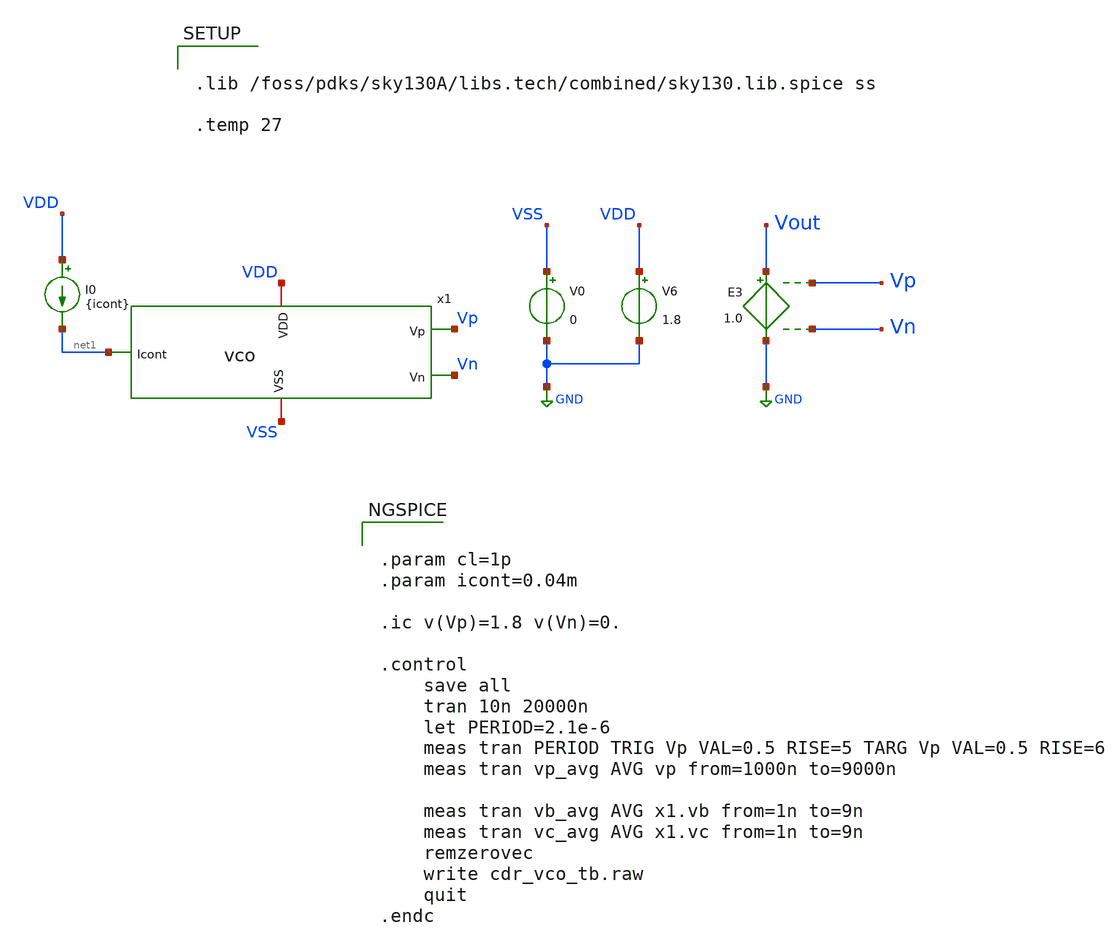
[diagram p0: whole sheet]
** sch_path: xschem/vco_tb.sch
**.subckt vco_tb
V0 VSS GND 0
V6 VDD GND 1.8
I0 VDD net1 {icont}
E3 Vout GND Vp Vn 1.0
x1 VDD VSS net1 Vp Vn vco
**** begin user architecture code


.param cl=1p
.param icont=0.04m

.ic v(Vp)=1.8 v(Vn)=0.

.control
	save all
	tran 10n 20000n
	let PERIOD=2.1e-6
	meas tran PERIOD TRIG Vp VAL=0.5 RISE=5 TARG Vp VAL=0.5 RISE=6
	meas tran vp_avg AVG vp from=1000n to=9000n

	meas tran vb_avg AVG x1.vb from=1n to=9n
	meas tran vc_avg AVG x1.vc from=1n to=9n
	remzerovec
	write cdr_vco_tb.raw
	quit
.endc




.lib /foss/pdks/sky130A/libs.tech/combined/sky130.lib.spice ss

.temp 27


**** end user architecture code
**.ends

* expanding   symbol:  vco.sym # of pins=5
** sym_path: xschem/vco.sym
** sch_path: xschem/vco.sch
.subckt vco VDD VSS Icont Vp Vn
*.iopin VDD
*.iopin VSS
*.ipin Icont
*.opin Vp
*.opin Vn
x1 VDD VSS Vp Vn Vb Vc net1 net2 vco_stage
x2 VDD VSS net1 net2 Vb Vc net3 net4 vco_stage
x3 VDD VSS net3 net4 Vb Vc Vpin1 Vnin1 vco_stage
x4 VDD VSS Vpin1 Vnin1 Vb Vc Vn Vp vco_stage
x5 VDD VSS Icont Vb Vc vco_bias
.ends


* expanding   symbol:  vco_stage.sym # of pins=8
** sym_path: xschem/vco_stage.sym
** sch_path: xschem/vco_stage.sch
.subckt vco_stage VDD VSS Vp Vn Vb Vc Vpout Vnout
*.iopin VDD
*.iopin VSS
*.ipin Vp
*.ipin Vn
*.ipin Vb
*.ipin Vc
*.opin Vpout
*.opin Vnout
XM5 Vds_m5 Vc VSS VSS sky130_fd_pr__nfet_01v8 L={L} W={W} nf=2 ad='int((nf+1)/2) * W/nf * 0.29' as='int((nf+2)/2) * W/nf * 0.29'
+ pd='2*int((nf+1)/2) * (W/nf + 0.29)' ps='2*int((nf+2)/2) * (W/nf + 0.29)' nrd='0.29 / W' nrs='0.29 / W'
+ sa=0 sb=0 sd=0 mult=1 m=1
x1 VDD VSS Vp Vb Vnout Vpout Vds_m5 vco_stage_half
x2 VDD VSS Vn Vb Vpout Vnout Vds_m5 vco_stage_half
.ends


* expanding   symbol:  vco_bias.sym # of pins=5
** sym_path: xschem/vco_bias.sym
** sch_path: xschem/vco_bias.sch
.subckt vco_bias VDD VSS Icont Vb Vc
*.iopin VDD
*.iopin VSS
*.ipin Icont
*.opin Vb
*.opin Vc
XM1 Icont Icont VSS VSS sky130_fd_pr__nfet_01v8 L=1 W=2 nf=2 ad='int((nf+1)/2) * W/nf * 0.29' as='int((nf+2)/2) * W/nf * 0.29'
+ pd='2*int((nf+1)/2) * (W/nf + 0.29)' ps='2*int((nf+2)/2) * (W/nf + 0.29)' nrd='0.29 / W' nrs='0.29 / W'
+ sa=0 sb=0 sd=0 mult=1 m=1
XM2 Vb Icont VSS VSS sky130_fd_pr__nfet_01v8 L=1 W=2 nf=2 ad='int((nf+1)/2) * W/nf * 0.29' as='int((nf+2)/2) * W/nf * 0.29'
+ pd='2*int((nf+1)/2) * (W/nf + 0.29)' ps='2*int((nf+2)/2) * (W/nf + 0.29)' nrd='0.29 / W' nrs='0.29 / W'
+ sa=0 sb=0 sd=0 mult=1 m=1
XM3 VDD Vb Vb VDD sky130_fd_pr__nfet_01v8 L=1 W=2 nf=2 ad='int((nf+1)/2) * W/nf * 0.29' as='int((nf+2)/2) * W/nf * 0.29'
+ pd='2*int((nf+1)/2) * (W/nf + 0.29)' ps='2*int((nf+2)/2) * (W/nf + 0.29)' nrd='0.29 / W' nrs='0.29 / W'
+ sa=0 sb=0 sd=0 mult=1 m=1
V1 Vc Icont 0
.ends


* expanding   symbol:  vco_stage_half.sym # of pins=7
** sym_path: xschem/vco_stage_half.sym
** sch_path: xschem/vco_stage_half.sch
.subckt vco_stage_half VDD VSS Vin Vb Vd Vout Vs
*.iopin VDD
*.iopin VSS
*.ipin Vin
*.ipin Vb
*.ipin Vd
*.opin Vout
*.opin Vs
XM8 VSS Vout VSS VSS sky130_fd_pr__nfet_01v8 L={WLcap} W={WLcap} nf=1 ad='int((nf+1)/2) * W/nf * 0.29'
+ as='int((nf+2)/2) * W/nf * 0.29' pd='2*int((nf+1)/2) * (W/nf + 0.29)' ps='2*int((nf+2)/2) * (W/nf + 0.29)'
+ nrd='0.29 / W' nrs='0.29 / W' sa=0 sb=0 sd=0 mult=1 m=1
XM7 Vout Vd VDD VDD sky130_fd_pr__pfet_01v8 L={L} W={W} nf=2 ad='int((nf+1)/2) * W/nf * 0.29' as='int((nf+2)/2) * W/nf * 0.29'
+ pd='2*int((nf+1)/2) * (W/nf + 0.29)' ps='2*int((nf+2)/2) * (W/nf + 0.29)' nrd='0.29 / W' nrs='0.29 / W'
+ sa=0 sb=0 sd=0 mult=1 m=1
XM3 Vout Vb VDD VDD sky130_fd_pr__pfet_01v8 L={L} W={W} nf=2 ad='int((nf+1)/2) * W/nf * 0.29' as='int((nf+2)/2) * W/nf * 0.29'
+ pd='2*int((nf+1)/2) * (W/nf + 0.29)' ps='2*int((nf+2)/2) * (W/nf + 0.29)' nrd='0.29 / W' nrs='0.29 / W'
+ sa=0 sb=0 sd=0 mult=1 m=1
XM1 Vout Vin Vs VSS sky130_fd_pr__nfet_01v8 L={L} W={W} nf=2 ad='int((nf+1)/2) * W/nf * 0.29' as='int((nf+2)/2) * W/nf * 0.29'
+ pd='2*int((nf+1)/2) * (W/nf + 0.29)' ps='2*int((nf+2)/2) * (W/nf + 0.29)' nrd='0.29 / W' nrs='0.29 / W'
+ sa=0 sb=0 sd=0 mult=1 m=1
.ends

.GLOBAL GND
.end
